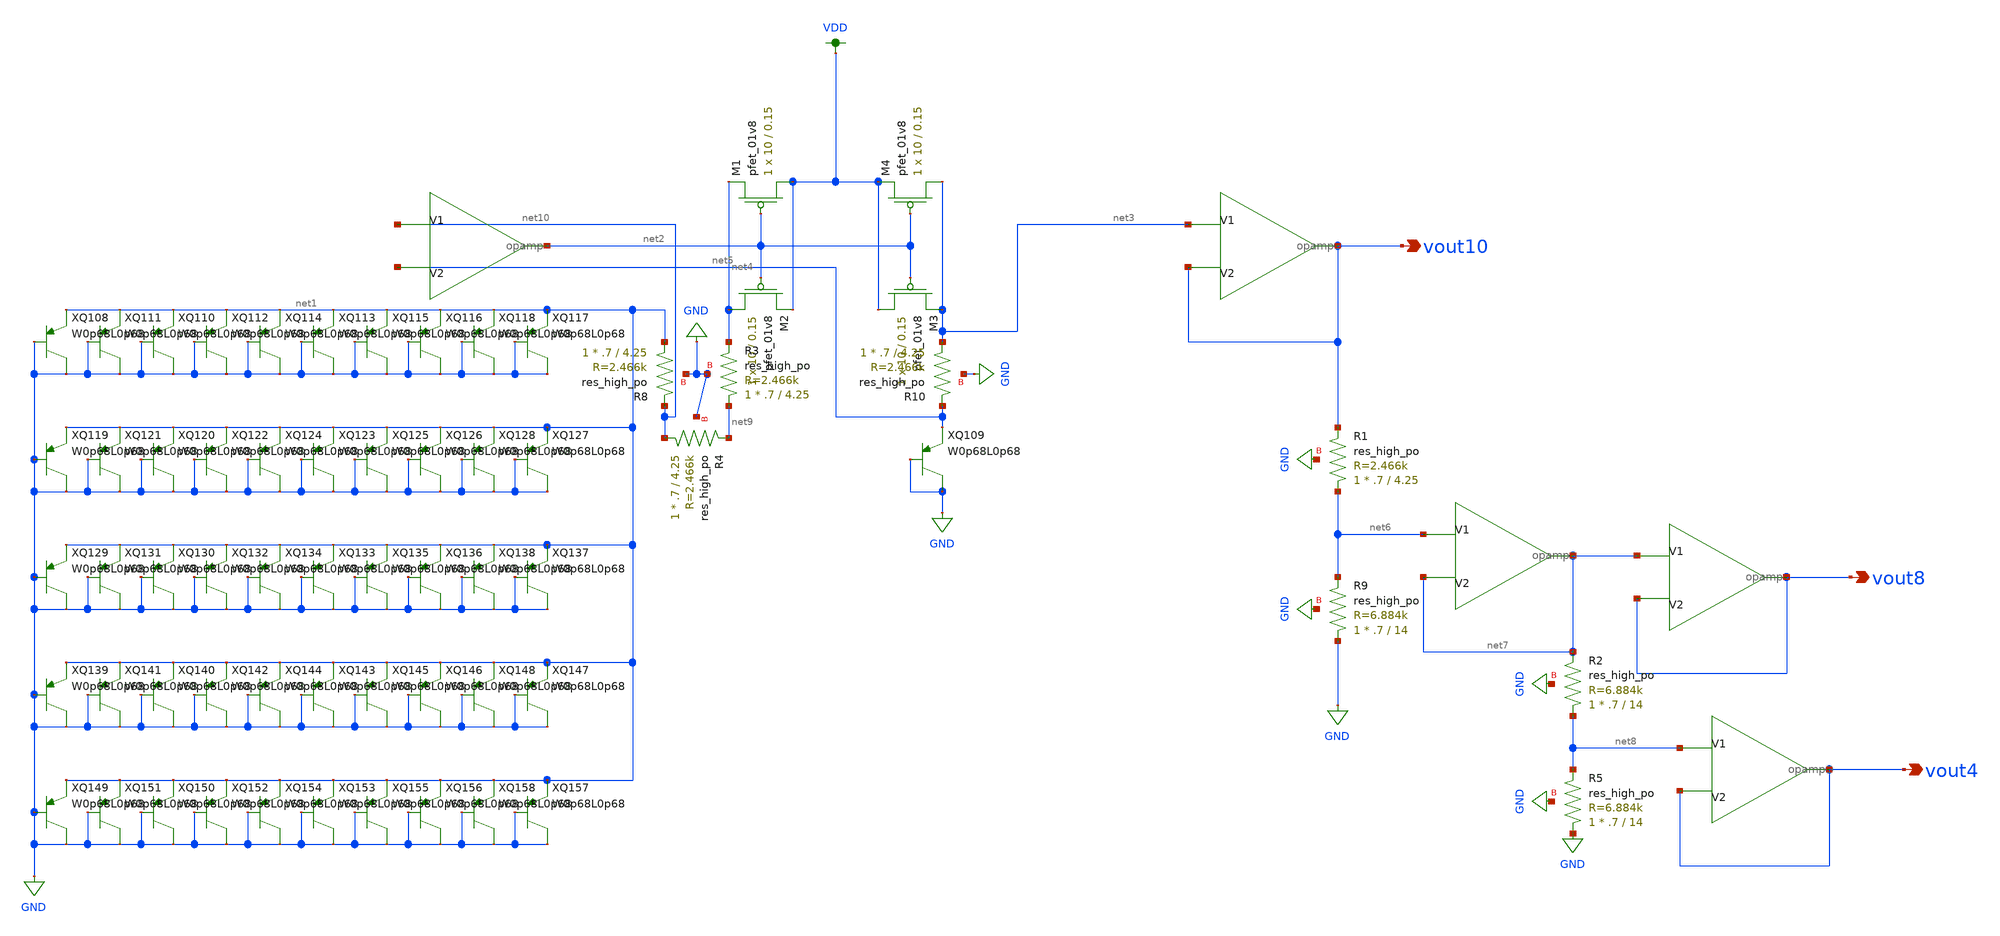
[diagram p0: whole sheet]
** sch_path: schematics/bandgap_LDS.sch
**.subckt bandgap_LDS vout10 vout8 vout4
*.opin vout10
*.opin vout8
*.opin vout4
XQ108 net1 GND GND sky130_fd_pr__pnp_05v0
XQ109 net5 GND GND sky130_fd_pr__pnp_05v0
XQ110 net1 GND GND sky130_fd_pr__pnp_05v0
XQ111 net1 GND GND sky130_fd_pr__pnp_05v0
XQ112 net1 GND GND sky130_fd_pr__pnp_05v0
XQ113 net1 GND GND sky130_fd_pr__pnp_05v0
XQ114 net1 GND GND sky130_fd_pr__pnp_05v0
XQ115 net1 GND GND sky130_fd_pr__pnp_05v0
XQ116 net1 GND GND sky130_fd_pr__pnp_05v0
XQ117 net1 GND GND sky130_fd_pr__pnp_05v0
XQ118 net1 GND GND sky130_fd_pr__pnp_05v0
XQ119 net1 GND GND sky130_fd_pr__pnp_05v0
XQ120 net1 GND GND sky130_fd_pr__pnp_05v0
XQ121 net1 GND GND sky130_fd_pr__pnp_05v0
XQ122 net1 GND GND sky130_fd_pr__pnp_05v0
XQ123 net1 GND GND sky130_fd_pr__pnp_05v0
XQ124 net1 GND GND sky130_fd_pr__pnp_05v0
XQ125 net1 GND GND sky130_fd_pr__pnp_05v0
XQ126 net1 GND GND sky130_fd_pr__pnp_05v0
XQ127 net1 GND GND sky130_fd_pr__pnp_05v0
XQ128 net1 GND GND sky130_fd_pr__pnp_05v0
XQ129 net1 GND GND sky130_fd_pr__pnp_05v0
XQ130 net1 GND GND sky130_fd_pr__pnp_05v0
XQ131 net1 GND GND sky130_fd_pr__pnp_05v0
XQ132 net1 GND GND sky130_fd_pr__pnp_05v0
XQ133 net1 GND GND sky130_fd_pr__pnp_05v0
XQ134 net1 GND GND sky130_fd_pr__pnp_05v0
XQ135 net1 GND GND sky130_fd_pr__pnp_05v0
XQ136 net1 GND GND sky130_fd_pr__pnp_05v0
XQ137 net1 GND GND sky130_fd_pr__pnp_05v0
XQ138 net1 GND GND sky130_fd_pr__pnp_05v0
XQ139 net1 GND GND sky130_fd_pr__pnp_05v0
XQ140 net1 GND GND sky130_fd_pr__pnp_05v0
XQ141 net1 GND GND sky130_fd_pr__pnp_05v0
XQ142 net1 GND GND sky130_fd_pr__pnp_05v0
XQ143 net1 GND GND sky130_fd_pr__pnp_05v0
XQ144 net1 GND GND sky130_fd_pr__pnp_05v0
XQ145 net1 GND GND sky130_fd_pr__pnp_05v0
XQ146 net1 GND GND sky130_fd_pr__pnp_05v0
XQ147 net1 GND GND sky130_fd_pr__pnp_05v0
XQ148 net1 GND GND sky130_fd_pr__pnp_05v0
XQ149 net1 GND GND sky130_fd_pr__pnp_05v0
XQ150 net1 GND GND sky130_fd_pr__pnp_05v0
XQ151 net1 GND GND sky130_fd_pr__pnp_05v0
XQ152 net1 GND GND sky130_fd_pr__pnp_05v0
XQ153 net1 GND GND sky130_fd_pr__pnp_05v0
XQ154 net1 GND GND sky130_fd_pr__pnp_05v0
XQ155 net1 GND GND sky130_fd_pr__pnp_05v0
XQ156 net1 GND GND sky130_fd_pr__pnp_05v0
XQ157 net1 GND GND sky130_fd_pr__pnp_05v0
XQ158 net1 GND GND sky130_fd_pr__pnp_05v0
XM1 VDD net2 net4 VDD sky130_fd_pr__pfet_01v8 L=0.15 W=10 nf=1 ad='int((nf+1)/2) * W/nf * 0.29' as='int((nf+2)/2) * W/nf * 0.29'
+ pd='2*int((nf+1)/2) * (W/nf + 0.29)' ps='2*int((nf+2)/2) * (W/nf + 0.29)' nrd='0.29 / W' nrs='0.29 / W'
+ sa=0 sb=0 sd=0 mult=1 m=1
XM2 net4 net2 VDD VDD sky130_fd_pr__pfet_01v8 L=0.15 W=10 nf=1 ad='int((nf+1)/2) * W/nf * 0.29' as='int((nf+2)/2) * W/nf * 0.29'
+ pd='2*int((nf+1)/2) * (W/nf + 0.29)' ps='2*int((nf+2)/2) * (W/nf + 0.29)' nrd='0.29 / W' nrs='0.29 / W'
+ sa=0 sb=0 sd=0 mult=1 m=1
XM3 VDD net2 net3 VDD sky130_fd_pr__pfet_01v8 L=0.15 W=10 nf=1 ad='int((nf+1)/2) * W/nf * 0.29' as='int((nf+2)/2) * W/nf * 0.29'
+ pd='2*int((nf+1)/2) * (W/nf + 0.29)' ps='2*int((nf+2)/2) * (W/nf + 0.29)' nrd='0.29 / W' nrs='0.29 / W'
+ sa=0 sb=0 sd=0 mult=1 m=1
XM4 net3 net2 VDD VDD sky130_fd_pr__pfet_01v8 L=0.15 W=10 nf=1 ad='int((nf+1)/2) * W/nf * 0.29' as='int((nf+2)/2) * W/nf * 0.29'
+ pd='2*int((nf+1)/2) * (W/nf + 0.29)' ps='2*int((nf+2)/2) * (W/nf + 0.29)' nrd='0.29 / W' nrs='0.29 / W'
+ sa=0 sb=0 sd=0 mult=1 m=1
X1 net10 net5 net2 opamp
X2 net3 vout10 vout10 opamp
X3 net6 net7 net7 opamp
X4 net8 vout4 vout4 opamp
X5 net7 vout8 vout8 opamp
XR8 net1 net10 GND sky130_fd_pr__res_high_po W=.7 L=4.25 mult=1 m=1
XR9 GND net6 GND sky130_fd_pr__res_high_po W=.7 L=14 mult=1 m=1
XR3 net9 net4 GND sky130_fd_pr__res_high_po W=.7 L=4.25 mult=1 m=1
XR4 net10 net9 GND sky130_fd_pr__res_high_po W=.7 L=4.25 mult=1 m=1
XR10 net3 net5 GND sky130_fd_pr__res_high_po W=.7 L=4.25 mult=1 m=1
XR1 net6 vout10 GND sky130_fd_pr__res_high_po W=.7 L=4.25 mult=1 m=1
XR2 net8 net7 GND sky130_fd_pr__res_high_po W=.7 L=14 mult=1 m=1
XR5 GND net8 GND sky130_fd_pr__res_high_po W=.7 L=14 mult=1 m=1
**.ends

* expanding   symbol:  /home/madvlsi/Desktop/MADVLSI_final/schematics/opamp.sym # of pins=3
** sym_path: schematics/opamp.sym
** sch_path: schematics/opamp.sch
.subckt opamp V1 V2 VOUT
*.ipin V1
*.ipin V2
*.opin VOUT
XM19 net12 net10 GND VDD sky130_fd_pr__pfet_01v8 L=.6 W=1.5 nf=1 ad='int((nf+1)/2) * W/nf * 0.29' as='int((nf+2)/2) * W/nf * 0.29'
+ pd='2*int((nf+1)/2) * (W/nf + 0.29)' ps='2*int((nf+2)/2) * (W/nf + 0.29)' nrd='0.29 / W' nrs='0.29 / W'
+ sa=0 sb=0 sd=0 mult=1 m=1
XMD20 VDD VDD net12 VDD sky130_fd_pr__pfet_01v8 L=.6 W=1.5 nf=1 ad='int((nf+1)/2) * W/nf * 0.29' as='int((nf+2)/2) * W/nf * 0.29'
+ pd='2*int((nf+1)/2) * (W/nf + 0.29)' ps='2*int((nf+2)/2) * (W/nf + 0.29)' nrd='0.29 / W' nrs='0.29 / W'
+ sa=0 sb=0 sd=0 mult=1 m=1
XM22 net12 net10 net9 VDD sky130_fd_pr__pfet_01v8 L=.6 W=1.5 nf=1 ad='int((nf+1)/2) * W/nf * 0.29' as='int((nf+2)/2) * W/nf * 0.29'
+ pd='2*int((nf+1)/2) * (W/nf + 0.29)' ps='2*int((nf+2)/2) * (W/nf + 0.29)' nrd='0.29 / W' nrs='0.29 / W'
+ sa=0 sb=0 sd=0 mult=1 m=1
XM23 GND net10 net12 VDD sky130_fd_pr__pfet_01v8 L=.6 W=1.5 nf=1 ad='int((nf+1)/2) * W/nf * 0.29' as='int((nf+2)/2) * W/nf * 0.29'
+ pd='2*int((nf+1)/2) * (W/nf + 0.29)' ps='2*int((nf+2)/2) * (W/nf + 0.29)' nrd='0.29 / W' nrs='0.29 / W'
+ sa=0 sb=0 sd=0 mult=1 m=1
XMD24 net9 VDD net10 VDD sky130_fd_pr__pfet_01v8 L=.6 W=1.5 nf=1 ad='int((nf+1)/2) * W/nf * 0.29' as='int((nf+2)/2) * W/nf * 0.29'
+ pd='2*int((nf+1)/2) * (W/nf + 0.29)' ps='2*int((nf+2)/2) * (W/nf + 0.29)' nrd='0.29 / W' nrs='0.29 / W'
+ sa=0 sb=0 sd=0 mult=1 m=1
XM25 VDD net10 net12 VDD sky130_fd_pr__pfet_01v8 L=.6 W=1.5 nf=1 ad='int((nf+1)/2) * W/nf * 0.29' as='int((nf+2)/2) * W/nf * 0.29'
+ pd='2*int((nf+1)/2) * (W/nf + 0.29)' ps='2*int((nf+2)/2) * (W/nf + 0.29)' nrd='0.29 / W' nrs='0.29 / W'
+ sa=0 sb=0 sd=0 mult=1 m=1
XM26 net7 V2 net11 VDD sky130_fd_pr__pfet_01v8 L=.6 W=1.5 nf=1 ad='int((nf+1)/2) * W/nf * 0.29' as='int((nf+2)/2) * W/nf * 0.29'
+ pd='2*int((nf+1)/2) * (W/nf + 0.29)' ps='2*int((nf+2)/2) * (W/nf + 0.29)' nrd='0.29 / W' nrs='0.29 / W'
+ sa=0 sb=0 sd=0 mult=1 m=1
XMD27 net5 VDD net14 VDD sky130_fd_pr__pfet_01v8 L=.6 W=1.5 nf=1 ad='int((nf+1)/2) * W/nf * 0.29' as='int((nf+2)/2) * W/nf * 0.29'
+ pd='2*int((nf+1)/2) * (W/nf + 0.29)' ps='2*int((nf+2)/2) * (W/nf + 0.29)' nrd='0.29 / W' nrs='0.29 / W'
+ sa=0 sb=0 sd=0 mult=1 m=1
XM28 net6 V1 net11 VDD sky130_fd_pr__pfet_01v8 L=.6 W=1.5 nf=1 ad='int((nf+1)/2) * W/nf * 0.29' as='int((nf+2)/2) * W/nf * 0.29'
+ pd='2*int((nf+1)/2) * (W/nf + 0.29)' ps='2*int((nf+2)/2) * (W/nf + 0.29)' nrd='0.29 / W' nrs='0.29 / W'
+ sa=0 sb=0 sd=0 mult=1 m=1
XM29 net11 net10 VDD VDD sky130_fd_pr__pfet_01v8 L=.6 W=1.5 nf=1 ad='int((nf+1)/2) * W/nf * 0.29' as='int((nf+2)/2) * W/nf * 0.29'
+ pd='2*int((nf+1)/2) * (W/nf + 0.29)' ps='2*int((nf+2)/2) * (W/nf + 0.29)' nrd='0.29 / W' nrs='0.29 / W'
+ sa=0 sb=0 sd=0 mult=1 m=1
XMD30 net11 VDD VDD VDD sky130_fd_pr__pfet_01v8 L=.6 W=1.5 nf=1 ad='int((nf+1)/2) * W/nf * 0.29' as='int((nf+2)/2) * W/nf * 0.29'
+ pd='2*int((nf+1)/2) * (W/nf + 0.29)' ps='2*int((nf+2)/2) * (W/nf + 0.29)' nrd='0.29 / W' nrs='0.29 / W'
+ sa=0 sb=0 sd=0 mult=1 m=1
XMD31 net2 VDD net13 VDD sky130_fd_pr__pfet_01v8 L=.6 W=1.5 nf=1 ad='int((nf+1)/2) * W/nf * 0.29' as='int((nf+2)/2) * W/nf * 0.29'
+ pd='2*int((nf+1)/2) * (W/nf + 0.29)' ps='2*int((nf+2)/2) * (W/nf + 0.29)' nrd='0.29 / W' nrs='0.29 / W'
+ sa=0 sb=0 sd=0 mult=1 m=1
XM32 net4 net5 net5 VDD sky130_fd_pr__pfet_01v8 L=.6 W=1.5 nf=1 ad='int((nf+1)/2) * W/nf * 0.29' as='int((nf+2)/2) * W/nf * 0.29'
+ pd='2*int((nf+1)/2) * (W/nf + 0.29)' ps='2*int((nf+2)/2) * (W/nf + 0.29)' nrd='0.29 / W' nrs='0.29 / W'
+ sa=0 sb=0 sd=0 mult=1 m=1
XM33 VDD net10 net4 VDD sky130_fd_pr__pfet_01v8 L=.6 W=1.5 nf=1 ad='int((nf+1)/2) * W/nf * 0.29' as='int((nf+2)/2) * W/nf * 0.29'
+ pd='2*int((nf+1)/2) * (W/nf + 0.29)' ps='2*int((nf+2)/2) * (W/nf + 0.29)' nrd='0.29 / W' nrs='0.29 / W'
+ sa=0 sb=0 sd=0 mult=1 m=1
XM34 net3 net5 net2 VDD sky130_fd_pr__pfet_01v8 L=.6 W=1.5 nf=1 ad='int((nf+1)/2) * W/nf * 0.29' as='int((nf+2)/2) * W/nf * 0.29'
+ pd='2*int((nf+1)/2) * (W/nf + 0.29)' ps='2*int((nf+2)/2) * (W/nf + 0.29)' nrd='0.29 / W' nrs='0.29 / W'
+ sa=0 sb=0 sd=0 mult=1 m=1
XM35 VDD net10 net3 VDD sky130_fd_pr__pfet_01v8 L=.6 W=1.5 nf=1 ad='int((nf+1)/2) * W/nf * 0.29' as='int((nf+2)/2) * W/nf * 0.29'
+ pd='2*int((nf+1)/2) * (W/nf + 0.29)' ps='2*int((nf+2)/2) * (W/nf + 0.29)' nrd='0.29 / W' nrs='0.29 / W'
+ sa=0 sb=0 sd=0 mult=1 m=1
XM36 VOUT net2 VDD VDD sky130_fd_pr__pfet_01v8 L=.6 W=1.5 nf=1 ad='int((nf+1)/2) * W/nf * 0.29' as='int((nf+2)/2) * W/nf * 0.29'
+ pd='2*int((nf+1)/2) * (W/nf + 0.29)' ps='2*int((nf+2)/2) * (W/nf + 0.29)' nrd='0.29 / W' nrs='0.29 / W'
+ sa=0 sb=0 sd=0 mult=1 m=1
XM37 VDD net2 VOUT VDD sky130_fd_pr__pfet_01v8 L=.6 W=1.5 nf=1 ad='int((nf+1)/2) * W/nf * 0.29' as='int((nf+2)/2) * W/nf * 0.29'
+ pd='2*int((nf+1)/2) * (W/nf + 0.29)' ps='2*int((nf+2)/2) * (W/nf + 0.29)' nrd='0.29 / W' nrs='0.29 / W'
+ sa=0 sb=0 sd=0 mult=1 m=1
XM38 VOUT net2 VDD VDD sky130_fd_pr__pfet_01v8 L=.6 W=1.5 nf=1 ad='int((nf+1)/2) * W/nf * 0.29' as='int((nf+2)/2) * W/nf * 0.29'
+ pd='2*int((nf+1)/2) * (W/nf + 0.29)' ps='2*int((nf+2)/2) * (W/nf + 0.29)' nrd='0.29 / W' nrs='0.29 / W'
+ sa=0 sb=0 sd=0 mult=1 m=1
XM39 VDD net2 VOUT VDD sky130_fd_pr__pfet_01v8 L=.6 W=1.5 nf=1 ad='int((nf+1)/2) * W/nf * 0.29' as='int((nf+2)/2) * W/nf * 0.29'
+ pd='2*int((nf+1)/2) * (W/nf + 0.29)' ps='2*int((nf+2)/2) * (W/nf + 0.29)' nrd='0.29 / W' nrs='0.29 / W'
+ sa=0 sb=0 sd=0 mult=1 m=1
XM40 net1 net9 VDD GND sky130_fd_pr__nfet_01v8 L=.6 W=1.5 nf=1 ad='int((nf+1)/2) * W/nf * 0.29' as='int((nf+2)/2) * W/nf * 0.29'
+ pd='2*int((nf+1)/2) * (W/nf + 0.29)' ps='2*int((nf+2)/2) * (W/nf + 0.29)' nrd='0.29 / W' nrs='0.29 / W'
+ sa=0 sb=0 sd=0 mult=1 m=1
XMD41 GND GND net1 GND sky130_fd_pr__nfet_01v8 L=.6 W=1.5 nf=1 ad='int((nf+1)/2) * W/nf * 0.29' as='int((nf+2)/2) * W/nf * 0.29'
+ pd='2*int((nf+1)/2) * (W/nf + 0.29)' ps='2*int((nf+2)/2) * (W/nf + 0.29)' nrd='0.29 / W' nrs='0.29 / W'
+ sa=0 sb=0 sd=0 mult=1 m=1
XM42 net1 net9 net10 GND sky130_fd_pr__nfet_01v8 L=.6 W=1.5 nf=1 ad='int((nf+1)/2) * W/nf * 0.29' as='int((nf+2)/2) * W/nf * 0.29'
+ pd='2*int((nf+1)/2) * (W/nf + 0.29)' ps='2*int((nf+2)/2) * (W/nf + 0.29)' nrd='0.29 / W' nrs='0.29 / W'
+ sa=0 sb=0 sd=0 mult=1 m=1
XM43 VDD net9 net1 GND sky130_fd_pr__nfet_01v8 L=.6 W=1.5 nf=1 ad='int((nf+1)/2) * W/nf * 0.29' as='int((nf+2)/2) * W/nf * 0.29'
+ pd='2*int((nf+1)/2) * (W/nf + 0.29)' ps='2*int((nf+2)/2) * (W/nf + 0.29)' nrd='0.29 / W' nrs='0.29 / W'
+ sa=0 sb=0 sd=0 mult=1 m=1
XMD44 net10 GND net9 GND sky130_fd_pr__nfet_01v8 L=.6 W=1.5 nf=1 ad='int((nf+1)/2) * W/nf * 0.29' as='int((nf+2)/2) * W/nf * 0.29'
+ pd='2*int((nf+1)/2) * (W/nf + 0.29)' ps='2*int((nf+2)/2) * (W/nf + 0.29)' nrd='0.29 / W' nrs='0.29 / W'
+ sa=0 sb=0 sd=0 mult=1 m=1
XM45 GND net9 net1 GND sky130_fd_pr__nfet_01v8 L=.6 W=1.5 nf=1 ad='int((nf+1)/2) * W/nf * 0.29' as='int((nf+2)/2) * W/nf * 0.29'
+ pd='2*int((nf+1)/2) * (W/nf + 0.29)' ps='2*int((nf+2)/2) * (W/nf + 0.29)' nrd='0.29 / W' nrs='0.29 / W'
+ sa=0 sb=0 sd=0 mult=1 m=1
XM46 net3 V1 net8 GND sky130_fd_pr__nfet_01v8 L=.6 W=1.5 nf=1 ad='int((nf+1)/2) * W/nf * 0.29' as='int((nf+2)/2) * W/nf * 0.29'
+ pd='2*int((nf+1)/2) * (W/nf + 0.29)' ps='2*int((nf+2)/2) * (W/nf + 0.29)' nrd='0.29 / W' nrs='0.29 / W'
+ sa=0 sb=0 sd=0 mult=1 m=1
XMD47 net5 GND net15 GND sky130_fd_pr__nfet_01v8 L=.6 W=1.5 nf=1 ad='int((nf+1)/2) * W/nf * 0.29' as='int((nf+2)/2) * W/nf * 0.29'
+ pd='2*int((nf+1)/2) * (W/nf + 0.29)' ps='2*int((nf+2)/2) * (W/nf + 0.29)' nrd='0.29 / W' nrs='0.29 / W'
+ sa=0 sb=0 sd=0 mult=1 m=1
XM48 net4 V2 net8 GND sky130_fd_pr__nfet_01v8 L=.6 W=1.5 nf=1 ad='int((nf+1)/2) * W/nf * 0.29' as='int((nf+2)/2) * W/nf * 0.29'
+ pd='2*int((nf+1)/2) * (W/nf + 0.29)' ps='2*int((nf+2)/2) * (W/nf + 0.29)' nrd='0.29 / W' nrs='0.29 / W'
+ sa=0 sb=0 sd=0 mult=1 m=1
XM49 net8 net9 GND GND sky130_fd_pr__nfet_01v8 L=.6 W=1.5 nf=1 ad='int((nf+1)/2) * W/nf * 0.29' as='int((nf+2)/2) * W/nf * 0.29'
+ pd='2*int((nf+1)/2) * (W/nf + 0.29)' ps='2*int((nf+2)/2) * (W/nf + 0.29)' nrd='0.29 / W' nrs='0.29 / W'
+ sa=0 sb=0 sd=0 mult=1 m=1
XMD50 net8 GND GND GND sky130_fd_pr__nfet_01v8 L=.6 W=1.5 nf=1 ad='int((nf+1)/2) * W/nf * 0.29' as='int((nf+2)/2) * W/nf * 0.29'
+ pd='2*int((nf+1)/2) * (W/nf + 0.29)' ps='2*int((nf+2)/2) * (W/nf + 0.29)' nrd='0.29 / W' nrs='0.29 / W'
+ sa=0 sb=0 sd=0 mult=1 m=1
XMD51 net2 GND net16 GND sky130_fd_pr__nfet_01v8 L=.6 W=1.5 nf=1 ad='int((nf+1)/2) * W/nf * 0.29' as='int((nf+2)/2) * W/nf * 0.29'
+ pd='2*int((nf+1)/2) * (W/nf + 0.29)' ps='2*int((nf+2)/2) * (W/nf + 0.29)' nrd='0.29 / W' nrs='0.29 / W'
+ sa=0 sb=0 sd=0 mult=1 m=1
XM52 GND net9 net7 GND sky130_fd_pr__nfet_01v8 L=.6 W=1.5 nf=1 ad='int((nf+1)/2) * W/nf * 0.29' as='int((nf+2)/2) * W/nf * 0.29'
+ pd='2*int((nf+1)/2) * (W/nf + 0.29)' ps='2*int((nf+2)/2) * (W/nf + 0.29)' nrd='0.29 / W' nrs='0.29 / W'
+ sa=0 sb=0 sd=0 mult=1 m=1
XMD53 VOUT GND GND GND sky130_fd_pr__nfet_01v8 L=.6 W=1.5 nf=1 ad='int((nf+1)/2) * W/nf * 0.29' as='int((nf+2)/2) * W/nf * 0.29'
+ pd='2*int((nf+1)/2) * (W/nf + 0.29)' ps='2*int((nf+2)/2) * (W/nf + 0.29)' nrd='0.29 / W' nrs='0.29 / W'
+ sa=0 sb=0 sd=0 mult=1 m=1
XM54 GND net9 net6 GND sky130_fd_pr__nfet_01v8 L=.6 W=1.5 nf=1 ad='int((nf+1)/2) * W/nf * 0.29' as='int((nf+2)/2) * W/nf * 0.29'
+ pd='2*int((nf+1)/2) * (W/nf + 0.29)' ps='2*int((nf+2)/2) * (W/nf + 0.29)' nrd='0.29 / W' nrs='0.29 / W'
+ sa=0 sb=0 sd=0 mult=1 m=1
XM55 net7 net5 net5 GND sky130_fd_pr__nfet_01v8 L=.6 W=1.5 nf=1 ad='int((nf+1)/2) * W/nf * 0.29' as='int((nf+2)/2) * W/nf * 0.29'
+ pd='2*int((nf+1)/2) * (W/nf + 0.29)' ps='2*int((nf+2)/2) * (W/nf + 0.29)' nrd='0.29 / W' nrs='0.29 / W'
+ sa=0 sb=0 sd=0 mult=1 m=1
XM56 net6 net5 net2 GND sky130_fd_pr__nfet_01v8 L=.6 W=1.5 nf=1 ad='int((nf+1)/2) * W/nf * 0.29' as='int((nf+2)/2) * W/nf * 0.29'
+ pd='2*int((nf+1)/2) * (W/nf + 0.29)' ps='2*int((nf+2)/2) * (W/nf + 0.29)' nrd='0.29 / W' nrs='0.29 / W'
+ sa=0 sb=0 sd=0 mult=1 m=1
XMD57 VOUT GND GND GND sky130_fd_pr__nfet_01v8 L=.6 W=1.5 nf=1 ad='int((nf+1)/2) * W/nf * 0.29' as='int((nf+2)/2) * W/nf * 0.29'
+ pd='2*int((nf+1)/2) * (W/nf + 0.29)' ps='2*int((nf+2)/2) * (W/nf + 0.29)' nrd='0.29 / W' nrs='0.29 / W'
+ sa=0 sb=0 sd=0 mult=1 m=1
XM58 GND net2 VOUT GND sky130_fd_pr__nfet_01v8 L=.6 W=1.5 nf=1 ad='int((nf+1)/2) * W/nf * 0.29' as='int((nf+2)/2) * W/nf * 0.29'
+ pd='2*int((nf+1)/2) * (W/nf + 0.29)' ps='2*int((nf+2)/2) * (W/nf + 0.29)' nrd='0.29 / W' nrs='0.29 / W'
+ sa=0 sb=0 sd=0 mult=1 m=1
XM59 GND net2 VOUT GND sky130_fd_pr__nfet_01v8 L=.6 W=1.5 nf=1 ad='int((nf+1)/2) * W/nf * 0.29' as='int((nf+2)/2) * W/nf * 0.29'
+ pd='2*int((nf+1)/2) * (W/nf + 0.29)' ps='2*int((nf+2)/2) * (W/nf + 0.29)' nrd='0.29 / W' nrs='0.29 / W'
+ sa=0 sb=0 sd=0 mult=1 m=1
XM60 net12 net10 GND VDD sky130_fd_pr__pfet_01v8 L=.6 W=1.5 nf=1 ad='int((nf+1)/2) * W/nf * 0.29' as='int((nf+2)/2) * W/nf * 0.29'
+ pd='2*int((nf+1)/2) * (W/nf + 0.29)' ps='2*int((nf+2)/2) * (W/nf + 0.29)' nrd='0.29 / W' nrs='0.29 / W'
+ sa=0 sb=0 sd=0 mult=1 m=1
XM61 net10 net10 net4 VDD sky130_fd_pr__pfet_01v8 L=.6 W=1.5 nf=1 ad='int((nf+1)/2) * W/nf * 0.29' as='int((nf+2)/2) * W/nf * 0.29'
+ pd='2*int((nf+1)/2) * (W/nf + 0.29)' ps='2*int((nf+2)/2) * (W/nf + 0.29)' nrd='0.29 / W' nrs='0.29 / W'
+ sa=0 sb=0 sd=0 mult=1 m=1
XM62 net1 net9 VDD GND sky130_fd_pr__nfet_01v8 L=.6 W=1.5 nf=1 ad='int((nf+1)/2) * W/nf * 0.29' as='int((nf+2)/2) * W/nf * 0.29'
+ pd='2*int((nf+1)/2) * (W/nf + 0.29)' ps='2*int((nf+2)/2) * (W/nf + 0.29)' nrd='0.29 / W' nrs='0.29 / W'
+ sa=0 sb=0 sd=0 mult=1 m=1
XM63 net9 net9 net7 GND sky130_fd_pr__nfet_01v8 L=.6 W=1.5 nf=1 ad='int((nf+1)/2) * W/nf * 0.29' as='int((nf+2)/2) * W/nf * 0.29'
+ pd='2*int((nf+1)/2) * (W/nf + 0.29)' ps='2*int((nf+2)/2) * (W/nf + 0.29)' nrd='0.29 / W' nrs='0.29 / W'
+ sa=0 sb=0 sd=0 mult=1 m=1
XMD64 VDD GND GND GND sky130_fd_pr__nfet_01v8 L=.6 W=1.5 nf=1 ad='int((nf+1)/2) * W/nf * 0.29' as='int((nf+2)/2) * W/nf * 0.29'
+ pd='2*int((nf+1)/2) * (W/nf + 0.29)' ps='2*int((nf+2)/2) * (W/nf + 0.29)' nrd='0.29 / W' nrs='0.29 / W'
+ sa=0 sb=0 sd=0 mult=1 m=1
XMD65 net7 GND GND GND sky130_fd_pr__nfet_01v8 L=.6 W=1.5 nf=1 ad='int((nf+1)/2) * W/nf * 0.29' as='int((nf+2)/2) * W/nf * 0.29'
+ pd='2*int((nf+1)/2) * (W/nf + 0.29)' ps='2*int((nf+2)/2) * (W/nf + 0.29)' nrd='0.29 / W' nrs='0.29 / W'
+ sa=0 sb=0 sd=0 mult=1 m=1
XMD66 GND VDD VDD VDD sky130_fd_pr__pfet_01v8 L=.6 W=1.5 nf=1 ad='int((nf+1)/2) * W/nf * 0.29' as='int((nf+2)/2) * W/nf * 0.29'
+ pd='2*int((nf+1)/2) * (W/nf + 0.29)' ps='2*int((nf+2)/2) * (W/nf + 0.29)' nrd='0.29 / W' nrs='0.29 / W'
+ sa=0 sb=0 sd=0 mult=1 m=1
XMD67 net4 VDD VDD VDD sky130_fd_pr__pfet_01v8 L=.6 W=1.5 nf=1 ad='int((nf+1)/2) * W/nf * 0.29' as='int((nf+2)/2) * W/nf * 0.29'
+ pd='2*int((nf+1)/2) * (W/nf + 0.29)' ps='2*int((nf+2)/2) * (W/nf + 0.29)' nrd='0.29 / W' nrs='0.29 / W'
+ sa=0 sb=0 sd=0 mult=1 m=1
XMD1 net15 GND net3 GND sky130_fd_pr__nfet_01v8 L=.6 W=1.5 nf=1 ad='int((nf+1)/2) * W/nf * 0.29' as='int((nf+2)/2) * W/nf * 0.29'
+ pd='2*int((nf+1)/2) * (W/nf + 0.29)' ps='2*int((nf+2)/2) * (W/nf + 0.29)' nrd='0.29 / W' nrs='0.29 / W'
+ sa=0 sb=0 sd=0 mult=1 m=1
XMD2 net16 GND net4 GND sky130_fd_pr__nfet_01v8 L=.6 W=1.5 nf=1 ad='int((nf+1)/2) * W/nf * 0.29' as='int((nf+2)/2) * W/nf * 0.29'
+ pd='2*int((nf+1)/2) * (W/nf + 0.29)' ps='2*int((nf+2)/2) * (W/nf + 0.29)' nrd='0.29 / W' nrs='0.29 / W'
+ sa=0 sb=0 sd=0 mult=1 m=1
XMD3 net13 VDD net6 VDD sky130_fd_pr__pfet_01v8 L=.6 W=1.5 nf=1 ad='int((nf+1)/2) * W/nf * 0.29' as='int((nf+2)/2) * W/nf * 0.29'
+ pd='2*int((nf+1)/2) * (W/nf + 0.29)' ps='2*int((nf+2)/2) * (W/nf + 0.29)' nrd='0.29 / W' nrs='0.29 / W'
+ sa=0 sb=0 sd=0 mult=1 m=1
XMD4 net14 VDD net7 VDD sky130_fd_pr__pfet_01v8 L=.6 W=1.5 nf=1 ad='int((nf+1)/2) * W/nf * 0.29' as='int((nf+2)/2) * W/nf * 0.29'
+ pd='2*int((nf+1)/2) * (W/nf + 0.29)' ps='2*int((nf+2)/2) * (W/nf + 0.29)' nrd='0.29 / W' nrs='0.29 / W'
+ sa=0 sb=0 sd=0 mult=1 m=1
XM1 net21 net10 GND VDD sky130_fd_pr__pfet_01v8 L=.6 W=1.5 nf=1 ad='int((nf+1)/2) * W/nf * 0.29' as='int((nf+2)/2) * W/nf * 0.29'
+ pd='2*int((nf+1)/2) * (W/nf + 0.29)' ps='2*int((nf+2)/2) * (W/nf + 0.29)' nrd='0.29 / W' nrs='0.29 / W'
+ sa=0 sb=0 sd=0 mult=1 m=1
XMD5 VDD VDD net21 VDD sky130_fd_pr__pfet_01v8 L=.6 W=1.5 nf=1 ad='int((nf+1)/2) * W/nf * 0.29' as='int((nf+2)/2) * W/nf * 0.29'
+ pd='2*int((nf+1)/2) * (W/nf + 0.29)' ps='2*int((nf+2)/2) * (W/nf + 0.29)' nrd='0.29 / W' nrs='0.29 / W'
+ sa=0 sb=0 sd=0 mult=1 m=1
XM6 net21 net10 net9 VDD sky130_fd_pr__pfet_01v8 L=.6 W=1.5 nf=1 ad='int((nf+1)/2) * W/nf * 0.29' as='int((nf+2)/2) * W/nf * 0.29'
+ pd='2*int((nf+1)/2) * (W/nf + 0.29)' ps='2*int((nf+2)/2) * (W/nf + 0.29)' nrd='0.29 / W' nrs='0.29 / W'
+ sa=0 sb=0 sd=0 mult=1 m=1
XM7 GND net10 net21 VDD sky130_fd_pr__pfet_01v8 L=.6 W=1.5 nf=1 ad='int((nf+1)/2) * W/nf * 0.29' as='int((nf+2)/2) * W/nf * 0.29'
+ pd='2*int((nf+1)/2) * (W/nf + 0.29)' ps='2*int((nf+2)/2) * (W/nf + 0.29)' nrd='0.29 / W' nrs='0.29 / W'
+ sa=0 sb=0 sd=0 mult=1 m=1
XMD8 net9 VDD net10 VDD sky130_fd_pr__pfet_01v8 L=.6 W=1.5 nf=1 ad='int((nf+1)/2) * W/nf * 0.29' as='int((nf+2)/2) * W/nf * 0.29'
+ pd='2*int((nf+1)/2) * (W/nf + 0.29)' ps='2*int((nf+2)/2) * (W/nf + 0.29)' nrd='0.29 / W' nrs='0.29 / W'
+ sa=0 sb=0 sd=0 mult=1 m=1
XM9 VDD net10 net21 VDD sky130_fd_pr__pfet_01v8 L=.6 W=1.5 nf=1 ad='int((nf+1)/2) * W/nf * 0.29' as='int((nf+2)/2) * W/nf * 0.29'
+ pd='2*int((nf+1)/2) * (W/nf + 0.29)' ps='2*int((nf+2)/2) * (W/nf + 0.29)' nrd='0.29 / W' nrs='0.29 / W'
+ sa=0 sb=0 sd=0 mult=1 m=1
XM10 net7 V2 net20 VDD sky130_fd_pr__pfet_01v8 L=.6 W=1.5 nf=1 ad='int((nf+1)/2) * W/nf * 0.29' as='int((nf+2)/2) * W/nf * 0.29'
+ pd='2*int((nf+1)/2) * (W/nf + 0.29)' ps='2*int((nf+2)/2) * (W/nf + 0.29)' nrd='0.29 / W' nrs='0.29 / W'
+ sa=0 sb=0 sd=0 mult=1 m=1
XMD11 net18 VDD net23 VDD sky130_fd_pr__pfet_01v8 L=.6 W=1.5 nf=1 ad='int((nf+1)/2) * W/nf * 0.29' as='int((nf+2)/2) * W/nf * 0.29'
+ pd='2*int((nf+1)/2) * (W/nf + 0.29)' ps='2*int((nf+2)/2) * (W/nf + 0.29)' nrd='0.29 / W' nrs='0.29 / W'
+ sa=0 sb=0 sd=0 mult=1 m=1
XM12 net6 V1 net20 VDD sky130_fd_pr__pfet_01v8 L=.6 W=1.5 nf=1 ad='int((nf+1)/2) * W/nf * 0.29' as='int((nf+2)/2) * W/nf * 0.29'
+ pd='2*int((nf+1)/2) * (W/nf + 0.29)' ps='2*int((nf+2)/2) * (W/nf + 0.29)' nrd='0.29 / W' nrs='0.29 / W'
+ sa=0 sb=0 sd=0 mult=1 m=1
XM13 net20 net10 VDD VDD sky130_fd_pr__pfet_01v8 L=.6 W=1.5 nf=1 ad='int((nf+1)/2) * W/nf * 0.29' as='int((nf+2)/2) * W/nf * 0.29'
+ pd='2*int((nf+1)/2) * (W/nf + 0.29)' ps='2*int((nf+2)/2) * (W/nf + 0.29)' nrd='0.29 / W' nrs='0.29 / W'
+ sa=0 sb=0 sd=0 mult=1 m=1
XMD14 net20 VDD VDD VDD sky130_fd_pr__pfet_01v8 L=.6 W=1.5 nf=1 ad='int((nf+1)/2) * W/nf * 0.29' as='int((nf+2)/2) * W/nf * 0.29'
+ pd='2*int((nf+1)/2) * (W/nf + 0.29)' ps='2*int((nf+2)/2) * (W/nf + 0.29)' nrd='0.29 / W' nrs='0.29 / W'
+ sa=0 sb=0 sd=0 mult=1 m=1
XMD15 net2 VDD net22 VDD sky130_fd_pr__pfet_01v8 L=.6 W=1.5 nf=1 ad='int((nf+1)/2) * W/nf * 0.29' as='int((nf+2)/2) * W/nf * 0.29'
+ pd='2*int((nf+1)/2) * (W/nf + 0.29)' ps='2*int((nf+2)/2) * (W/nf + 0.29)' nrd='0.29 / W' nrs='0.29 / W'
+ sa=0 sb=0 sd=0 mult=1 m=1
XM16 net4 net18 net18 VDD sky130_fd_pr__pfet_01v8 L=.6 W=1.5 nf=1 ad='int((nf+1)/2) * W/nf * 0.29' as='int((nf+2)/2) * W/nf * 0.29'
+ pd='2*int((nf+1)/2) * (W/nf + 0.29)' ps='2*int((nf+2)/2) * (W/nf + 0.29)' nrd='0.29 / W' nrs='0.29 / W'
+ sa=0 sb=0 sd=0 mult=1 m=1
XM17 VDD net10 net4 VDD sky130_fd_pr__pfet_01v8 L=.6 W=1.5 nf=1 ad='int((nf+1)/2) * W/nf * 0.29' as='int((nf+2)/2) * W/nf * 0.29'
+ pd='2*int((nf+1)/2) * (W/nf + 0.29)' ps='2*int((nf+2)/2) * (W/nf + 0.29)' nrd='0.29 / W' nrs='0.29 / W'
+ sa=0 sb=0 sd=0 mult=1 m=1
XM18 net3 net18 net2 VDD sky130_fd_pr__pfet_01v8 L=.6 W=1.5 nf=1 ad='int((nf+1)/2) * W/nf * 0.29' as='int((nf+2)/2) * W/nf * 0.29'
+ pd='2*int((nf+1)/2) * (W/nf + 0.29)' ps='2*int((nf+2)/2) * (W/nf + 0.29)' nrd='0.29 / W' nrs='0.29 / W'
+ sa=0 sb=0 sd=0 mult=1 m=1
XM20 VDD net10 net3 VDD sky130_fd_pr__pfet_01v8 L=.6 W=1.5 nf=1 ad='int((nf+1)/2) * W/nf * 0.29' as='int((nf+2)/2) * W/nf * 0.29'
+ pd='2*int((nf+1)/2) * (W/nf + 0.29)' ps='2*int((nf+2)/2) * (W/nf + 0.29)' nrd='0.29 / W' nrs='0.29 / W'
+ sa=0 sb=0 sd=0 mult=1 m=1
XM21 VOUT net2 VDD VDD sky130_fd_pr__pfet_01v8 L=.6 W=1.5 nf=1 ad='int((nf+1)/2) * W/nf * 0.29' as='int((nf+2)/2) * W/nf * 0.29'
+ pd='2*int((nf+1)/2) * (W/nf + 0.29)' ps='2*int((nf+2)/2) * (W/nf + 0.29)' nrd='0.29 / W' nrs='0.29 / W'
+ sa=0 sb=0 sd=0 mult=1 m=1
XM24 VDD net2 VOUT VDD sky130_fd_pr__pfet_01v8 L=.6 W=1.5 nf=1 ad='int((nf+1)/2) * W/nf * 0.29' as='int((nf+2)/2) * W/nf * 0.29'
+ pd='2*int((nf+1)/2) * (W/nf + 0.29)' ps='2*int((nf+2)/2) * (W/nf + 0.29)' nrd='0.29 / W' nrs='0.29 / W'
+ sa=0 sb=0 sd=0 mult=1 m=1
XM27 VOUT net2 VDD VDD sky130_fd_pr__pfet_01v8 L=.6 W=1.5 nf=1 ad='int((nf+1)/2) * W/nf * 0.29' as='int((nf+2)/2) * W/nf * 0.29'
+ pd='2*int((nf+1)/2) * (W/nf + 0.29)' ps='2*int((nf+2)/2) * (W/nf + 0.29)' nrd='0.29 / W' nrs='0.29 / W'
+ sa=0 sb=0 sd=0 mult=1 m=1
XM30 VDD net2 VOUT VDD sky130_fd_pr__pfet_01v8 L=.6 W=1.5 nf=1 ad='int((nf+1)/2) * W/nf * 0.29' as='int((nf+2)/2) * W/nf * 0.29'
+ pd='2*int((nf+1)/2) * (W/nf + 0.29)' ps='2*int((nf+2)/2) * (W/nf + 0.29)' nrd='0.29 / W' nrs='0.29 / W'
+ sa=0 sb=0 sd=0 mult=1 m=1
XM31 net17 net9 VDD GND sky130_fd_pr__nfet_01v8 L=.6 W=1.5 nf=1 ad='int((nf+1)/2) * W/nf * 0.29' as='int((nf+2)/2) * W/nf * 0.29'
+ pd='2*int((nf+1)/2) * (W/nf + 0.29)' ps='2*int((nf+2)/2) * (W/nf + 0.29)' nrd='0.29 / W' nrs='0.29 / W'
+ sa=0 sb=0 sd=0 mult=1 m=1
XMD32 GND GND net17 GND sky130_fd_pr__nfet_01v8 L=.6 W=1.5 nf=1 ad='int((nf+1)/2) * W/nf * 0.29' as='int((nf+2)/2) * W/nf * 0.29'
+ pd='2*int((nf+1)/2) * (W/nf + 0.29)' ps='2*int((nf+2)/2) * (W/nf + 0.29)' nrd='0.29 / W' nrs='0.29 / W'
+ sa=0 sb=0 sd=0 mult=1 m=1
XM41 net17 net9 net10 GND sky130_fd_pr__nfet_01v8 L=.6 W=1.5 nf=1 ad='int((nf+1)/2) * W/nf * 0.29' as='int((nf+2)/2) * W/nf * 0.29'
+ pd='2*int((nf+1)/2) * (W/nf + 0.29)' ps='2*int((nf+2)/2) * (W/nf + 0.29)' nrd='0.29 / W' nrs='0.29 / W'
+ sa=0 sb=0 sd=0 mult=1 m=1
XM44 VDD net9 net17 GND sky130_fd_pr__nfet_01v8 L=.6 W=1.5 nf=1 ad='int((nf+1)/2) * W/nf * 0.29' as='int((nf+2)/2) * W/nf * 0.29'
+ pd='2*int((nf+1)/2) * (W/nf + 0.29)' ps='2*int((nf+2)/2) * (W/nf + 0.29)' nrd='0.29 / W' nrs='0.29 / W'
+ sa=0 sb=0 sd=0 mult=1 m=1
XMD45 net10 GND net9 GND sky130_fd_pr__nfet_01v8 L=.6 W=1.5 nf=1 ad='int((nf+1)/2) * W/nf * 0.29' as='int((nf+2)/2) * W/nf * 0.29'
+ pd='2*int((nf+1)/2) * (W/nf + 0.29)' ps='2*int((nf+2)/2) * (W/nf + 0.29)' nrd='0.29 / W' nrs='0.29 / W'
+ sa=0 sb=0 sd=0 mult=1 m=1
XM47 GND net9 net17 GND sky130_fd_pr__nfet_01v8 L=.6 W=1.5 nf=1 ad='int((nf+1)/2) * W/nf * 0.29' as='int((nf+2)/2) * W/nf * 0.29'
+ pd='2*int((nf+1)/2) * (W/nf + 0.29)' ps='2*int((nf+2)/2) * (W/nf + 0.29)' nrd='0.29 / W' nrs='0.29 / W'
+ sa=0 sb=0 sd=0 mult=1 m=1
XM50 net3 V1 net19 GND sky130_fd_pr__nfet_01v8 L=.6 W=1.5 nf=1 ad='int((nf+1)/2) * W/nf * 0.29' as='int((nf+2)/2) * W/nf * 0.29'
+ pd='2*int((nf+1)/2) * (W/nf + 0.29)' ps='2*int((nf+2)/2) * (W/nf + 0.29)' nrd='0.29 / W' nrs='0.29 / W'
+ sa=0 sb=0 sd=0 mult=1 m=1
XMD52 net18 GND net24 GND sky130_fd_pr__nfet_01v8 L=.6 W=1.5 nf=1 ad='int((nf+1)/2) * W/nf * 0.29' as='int((nf+2)/2) * W/nf * 0.29'
+ pd='2*int((nf+1)/2) * (W/nf + 0.29)' ps='2*int((nf+2)/2) * (W/nf + 0.29)' nrd='0.29 / W' nrs='0.29 / W'
+ sa=0 sb=0 sd=0 mult=1 m=1
XM53 net4 V2 net19 GND sky130_fd_pr__nfet_01v8 L=.6 W=1.5 nf=1 ad='int((nf+1)/2) * W/nf * 0.29' as='int((nf+2)/2) * W/nf * 0.29'
+ pd='2*int((nf+1)/2) * (W/nf + 0.29)' ps='2*int((nf+2)/2) * (W/nf + 0.29)' nrd='0.29 / W' nrs='0.29 / W'
+ sa=0 sb=0 sd=0 mult=1 m=1
XM57 net19 net9 GND GND sky130_fd_pr__nfet_01v8 L=.6 W=1.5 nf=1 ad='int((nf+1)/2) * W/nf * 0.29' as='int((nf+2)/2) * W/nf * 0.29'
+ pd='2*int((nf+1)/2) * (W/nf + 0.29)' ps='2*int((nf+2)/2) * (W/nf + 0.29)' nrd='0.29 / W' nrs='0.29 / W'
+ sa=0 sb=0 sd=0 mult=1 m=1
XMD58 net19 GND GND GND sky130_fd_pr__nfet_01v8 L=.6 W=1.5 nf=1 ad='int((nf+1)/2) * W/nf * 0.29' as='int((nf+2)/2) * W/nf * 0.29'
+ pd='2*int((nf+1)/2) * (W/nf + 0.29)' ps='2*int((nf+2)/2) * (W/nf + 0.29)' nrd='0.29 / W' nrs='0.29 / W'
+ sa=0 sb=0 sd=0 mult=1 m=1
XMD59 net2 GND net25 GND sky130_fd_pr__nfet_01v8 L=.6 W=1.5 nf=1 ad='int((nf+1)/2) * W/nf * 0.29' as='int((nf+2)/2) * W/nf * 0.29'
+ pd='2*int((nf+1)/2) * (W/nf + 0.29)' ps='2*int((nf+2)/2) * (W/nf + 0.29)' nrd='0.29 / W' nrs='0.29 / W'
+ sa=0 sb=0 sd=0 mult=1 m=1
XM64 GND net9 net7 GND sky130_fd_pr__nfet_01v8 L=.6 W=1.5 nf=1 ad='int((nf+1)/2) * W/nf * 0.29' as='int((nf+2)/2) * W/nf * 0.29'
+ pd='2*int((nf+1)/2) * (W/nf + 0.29)' ps='2*int((nf+2)/2) * (W/nf + 0.29)' nrd='0.29 / W' nrs='0.29 / W'
+ sa=0 sb=0 sd=0 mult=1 m=1
XMD68 VOUT GND GND GND sky130_fd_pr__nfet_01v8 L=.6 W=1.5 nf=1 ad='int((nf+1)/2) * W/nf * 0.29' as='int((nf+2)/2) * W/nf * 0.29'
+ pd='2*int((nf+1)/2) * (W/nf + 0.29)' ps='2*int((nf+2)/2) * (W/nf + 0.29)' nrd='0.29 / W' nrs='0.29 / W'
+ sa=0 sb=0 sd=0 mult=1 m=1
XM69 GND net9 net6 GND sky130_fd_pr__nfet_01v8 L=.6 W=1.5 nf=1 ad='int((nf+1)/2) * W/nf * 0.29' as='int((nf+2)/2) * W/nf * 0.29'
+ pd='2*int((nf+1)/2) * (W/nf + 0.29)' ps='2*int((nf+2)/2) * (W/nf + 0.29)' nrd='0.29 / W' nrs='0.29 / W'
+ sa=0 sb=0 sd=0 mult=1 m=1
XM70 net7 net18 net18 GND sky130_fd_pr__nfet_01v8 L=.6 W=1.5 nf=1 ad='int((nf+1)/2) * W/nf * 0.29' as='int((nf+2)/2) * W/nf * 0.29'
+ pd='2*int((nf+1)/2) * (W/nf + 0.29)' ps='2*int((nf+2)/2) * (W/nf + 0.29)' nrd='0.29 / W' nrs='0.29 / W'
+ sa=0 sb=0 sd=0 mult=1 m=1
XM71 net6 net18 net2 GND sky130_fd_pr__nfet_01v8 L=.6 W=1.5 nf=1 ad='int((nf+1)/2) * W/nf * 0.29' as='int((nf+2)/2) * W/nf * 0.29'
+ pd='2*int((nf+1)/2) * (W/nf + 0.29)' ps='2*int((nf+2)/2) * (W/nf + 0.29)' nrd='0.29 / W' nrs='0.29 / W'
+ sa=0 sb=0 sd=0 mult=1 m=1
XMD72 VOUT GND GND GND sky130_fd_pr__nfet_01v8 L=.6 W=1.5 nf=1 ad='int((nf+1)/2) * W/nf * 0.29' as='int((nf+2)/2) * W/nf * 0.29'
+ pd='2*int((nf+1)/2) * (W/nf + 0.29)' ps='2*int((nf+2)/2) * (W/nf + 0.29)' nrd='0.29 / W' nrs='0.29 / W'
+ sa=0 sb=0 sd=0 mult=1 m=1
XM73 GND net2 VOUT GND sky130_fd_pr__nfet_01v8 L=.6 W=1.5 nf=1 ad='int((nf+1)/2) * W/nf * 0.29' as='int((nf+2)/2) * W/nf * 0.29'
+ pd='2*int((nf+1)/2) * (W/nf + 0.29)' ps='2*int((nf+2)/2) * (W/nf + 0.29)' nrd='0.29 / W' nrs='0.29 / W'
+ sa=0 sb=0 sd=0 mult=1 m=1
XM74 GND net2 VOUT GND sky130_fd_pr__nfet_01v8 L=.6 W=1.5 nf=1 ad='int((nf+1)/2) * W/nf * 0.29' as='int((nf+2)/2) * W/nf * 0.29'
+ pd='2*int((nf+1)/2) * (W/nf + 0.29)' ps='2*int((nf+2)/2) * (W/nf + 0.29)' nrd='0.29 / W' nrs='0.29 / W'
+ sa=0 sb=0 sd=0 mult=1 m=1
XM75 net21 net10 GND VDD sky130_fd_pr__pfet_01v8 L=.6 W=1.5 nf=1 ad='int((nf+1)/2) * W/nf * 0.29' as='int((nf+2)/2) * W/nf * 0.29'
+ pd='2*int((nf+1)/2) * (W/nf + 0.29)' ps='2*int((nf+2)/2) * (W/nf + 0.29)' nrd='0.29 / W' nrs='0.29 / W'
+ sa=0 sb=0 sd=0 mult=1 m=1
XM76 net10 net10 net4 VDD sky130_fd_pr__pfet_01v8 L=.6 W=1.5 nf=1 ad='int((nf+1)/2) * W/nf * 0.29' as='int((nf+2)/2) * W/nf * 0.29'
+ pd='2*int((nf+1)/2) * (W/nf + 0.29)' ps='2*int((nf+2)/2) * (W/nf + 0.29)' nrd='0.29 / W' nrs='0.29 / W'
+ sa=0 sb=0 sd=0 mult=1 m=1
XM77 net17 net9 VDD GND sky130_fd_pr__nfet_01v8 L=.6 W=1.5 nf=1 ad='int((nf+1)/2) * W/nf * 0.29' as='int((nf+2)/2) * W/nf * 0.29'
+ pd='2*int((nf+1)/2) * (W/nf + 0.29)' ps='2*int((nf+2)/2) * (W/nf + 0.29)' nrd='0.29 / W' nrs='0.29 / W'
+ sa=0 sb=0 sd=0 mult=1 m=1
XM78 net9 net9 net7 GND sky130_fd_pr__nfet_01v8 L=.6 W=1.5 nf=1 ad='int((nf+1)/2) * W/nf * 0.29' as='int((nf+2)/2) * W/nf * 0.29'
+ pd='2*int((nf+1)/2) * (W/nf + 0.29)' ps='2*int((nf+2)/2) * (W/nf + 0.29)' nrd='0.29 / W' nrs='0.29 / W'
+ sa=0 sb=0 sd=0 mult=1 m=1
XMD79 VDD GND GND GND sky130_fd_pr__nfet_01v8 L=.6 W=1.5 nf=1 ad='int((nf+1)/2) * W/nf * 0.29' as='int((nf+2)/2) * W/nf * 0.29'
+ pd='2*int((nf+1)/2) * (W/nf + 0.29)' ps='2*int((nf+2)/2) * (W/nf + 0.29)' nrd='0.29 / W' nrs='0.29 / W'
+ sa=0 sb=0 sd=0 mult=1 m=1
XMD80 net7 GND GND GND sky130_fd_pr__nfet_01v8 L=.6 W=1.5 nf=1 ad='int((nf+1)/2) * W/nf * 0.29' as='int((nf+2)/2) * W/nf * 0.29'
+ pd='2*int((nf+1)/2) * (W/nf + 0.29)' ps='2*int((nf+2)/2) * (W/nf + 0.29)' nrd='0.29 / W' nrs='0.29 / W'
+ sa=0 sb=0 sd=0 mult=1 m=1
XMD81 GND VDD VDD VDD sky130_fd_pr__pfet_01v8 L=.6 W=1.5 nf=1 ad='int((nf+1)/2) * W/nf * 0.29' as='int((nf+2)/2) * W/nf * 0.29'
+ pd='2*int((nf+1)/2) * (W/nf + 0.29)' ps='2*int((nf+2)/2) * (W/nf + 0.29)' nrd='0.29 / W' nrs='0.29 / W'
+ sa=0 sb=0 sd=0 mult=1 m=1
XMD82 net4 VDD VDD VDD sky130_fd_pr__pfet_01v8 L=.6 W=1.5 nf=1 ad='int((nf+1)/2) * W/nf * 0.29' as='int((nf+2)/2) * W/nf * 0.29'
+ pd='2*int((nf+1)/2) * (W/nf + 0.29)' ps='2*int((nf+2)/2) * (W/nf + 0.29)' nrd='0.29 / W' nrs='0.29 / W'
+ sa=0 sb=0 sd=0 mult=1 m=1
XMD83 net24 GND net3 GND sky130_fd_pr__nfet_01v8 L=.6 W=1.5 nf=1 ad='int((nf+1)/2) * W/nf * 0.29' as='int((nf+2)/2) * W/nf * 0.29'
+ pd='2*int((nf+1)/2) * (W/nf + 0.29)' ps='2*int((nf+2)/2) * (W/nf + 0.29)' nrd='0.29 / W' nrs='0.29 / W'
+ sa=0 sb=0 sd=0 mult=1 m=1
XMD84 net25 GND net4 GND sky130_fd_pr__nfet_01v8 L=.6 W=1.5 nf=1 ad='int((nf+1)/2) * W/nf * 0.29' as='int((nf+2)/2) * W/nf * 0.29'
+ pd='2*int((nf+1)/2) * (W/nf + 0.29)' ps='2*int((nf+2)/2) * (W/nf + 0.29)' nrd='0.29 / W' nrs='0.29 / W'
+ sa=0 sb=0 sd=0 mult=1 m=1
XMD85 net22 VDD net6 VDD sky130_fd_pr__pfet_01v8 L=.6 W=1.5 nf=1 ad='int((nf+1)/2) * W/nf * 0.29' as='int((nf+2)/2) * W/nf * 0.29'
+ pd='2*int((nf+1)/2) * (W/nf + 0.29)' ps='2*int((nf+2)/2) * (W/nf + 0.29)' nrd='0.29 / W' nrs='0.29 / W'
+ sa=0 sb=0 sd=0 mult=1 m=1
XMD86 net23 VDD net7 VDD sky130_fd_pr__pfet_01v8 L=.6 W=1.5 nf=1 ad='int((nf+1)/2) * W/nf * 0.29' as='int((nf+2)/2) * W/nf * 0.29'
+ pd='2*int((nf+1)/2) * (W/nf + 0.29)' ps='2*int((nf+2)/2) * (W/nf + 0.29)' nrd='0.29 / W' nrs='0.29 / W'
+ sa=0 sb=0 sd=0 mult=1 m=1
XC1 net2 VOUT sky130_fd_pr__cap_mim_m3_1 W=20 L=12 MF=1 m=1
.ends

.GLOBAL GND
.GLOBAL VDD
.end
